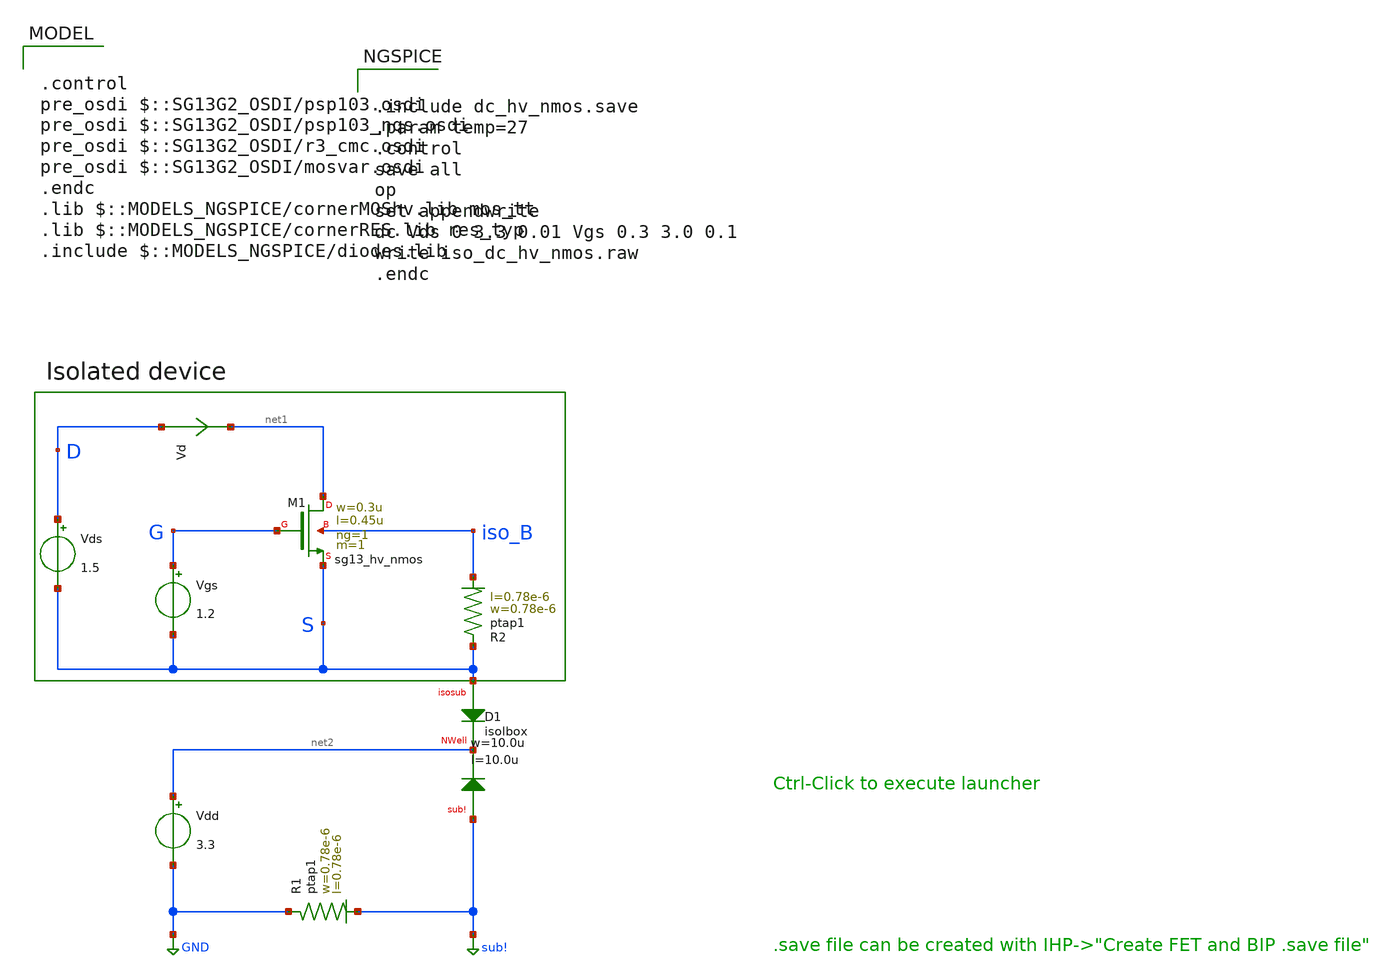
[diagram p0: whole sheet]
** sch_path: ihp-sg13g2/xschem_libs/sg13g2_tests/iso_dc_hv_nmos/schematic/iso_dc_hv_nmos.sch
* Copyright 2023 IHP PDK Authors
**.subckt iso_dc_hv_nmos
Vgs G S 1.2
Vds D S 1.5
Vd D net1 0
.save i(vd)
XD1 S net2 sub! isolbox l=10.0u w=10.0u
XR1 GND sub! ptap1 R=262.8 w=0.78e-6 l=0.78e-6
XR2 S iso_B ptap1 R=262.8 w=0.78e-6 l=0.78e-6
Vdd net2 GND 3.3
XM1 net1 G S iso_B sg13_hv_nmos w=0.3u l=0.45u ng=1 m=1 mm_ok=1
**** begin user architecture code

.control
pre_osdi $::SG13G2_OSDI/psp103.osdi
pre_osdi $::SG13G2_OSDI/psp103_nqs.osdi
pre_osdi $::SG13G2_OSDI/r3_cmc.osdi
pre_osdi $::SG13G2_OSDI/mosvar.osdi
.endc
.lib $::MODELS_NGSPICE/cornerMOShv.lib mos_tt
.lib $::MODELS_NGSPICE/cornerRES.lib res_typ
.include $::MODELS_NGSPICE/diodes.lib



.include dc_hv_nmos.save
.param temp=27
.control
save all
op
set appendwrite
dc Vds 0 3.3 0.01 Vgs 0.3 3.0 0.1
write iso_dc_hv_nmos.raw
.endc


**** end user architecture code
**.ends
.GLOBAL GND
.GLOBAL sub!
.end
